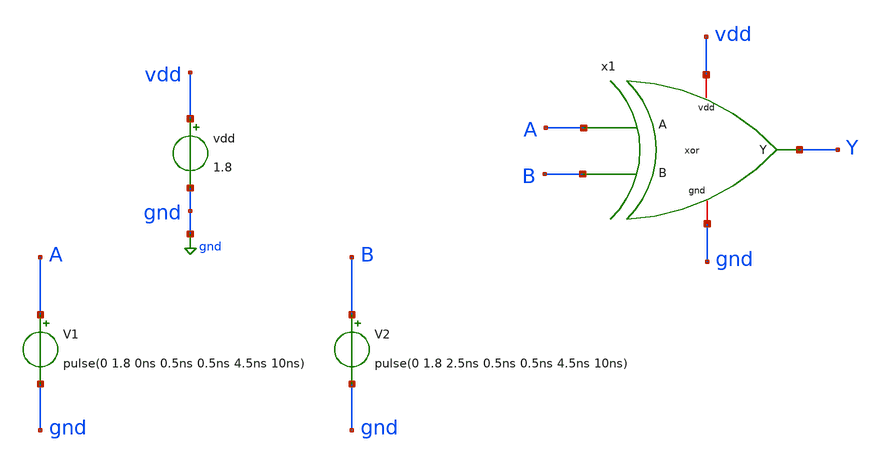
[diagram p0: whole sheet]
** sch_path: LogicGates/xor_tb.sch
**.subckt xor_tb
x1 vdd gnd A B Y xor
vdd vdd gnd 1.8
V1 A gnd pulse(0 1.8 0ns 0.5ns 0.5ns 4.5ns 10ns)
V2 B gnd pulse(0 1.8 2.5ns 0.5ns 0.5ns 4.5ns 10ns)
**** begin user architecture code


.lib /usr/local/share/pdk/sky130A/libs.tech/ngspice/sky130.lib.spice tt
.control
    tran 0.1n 100n
    plot A B
    plot Y
.endc

.save all

**** end user architecture code
**.ends

* expanding   symbol:  LogicGates/xor.sym # of pins=5
** sym_path: LogicGates/xor.sym
** sch_path: LogicGates/xor.sch
.subckt xor vdd gnd A B Y
*.ipin A
*.ipin B
*.iopin vdd
*.iopin gnd
*.opin Y
x1 vdd gnd A_c B net1 and
x2 vdd gnd A B_c net2 and
x3 vdd gnd net1 net2 Y or
x4 vdd gnd B B_c not
x5 vdd gnd A A_c not
.ends


* expanding   symbol:  LogicGates/and.sym # of pins=5
** sym_path: LogicGates/and.sym
** sch_path: LogicGates/and.sch
.subckt and vdd gnd A B Y
*.ipin A
*.ipin B
*.iopin vdd
*.iopin gnd
*.opin Y
XM1 net1 A net2 gnd sky130_fd_pr__nfet_01v8 L=0.15 W=1 nf=1 ad='int((nf+1)/2) * W/nf * 0.29' as='int((nf+2)/2) * W/nf * 0.29'
+ pd='2*int((nf+1)/2) * (W/nf + 0.29)' ps='2*int((nf+2)/2) * (W/nf + 0.29)' nrd='0.29 / W' nrs='0.29 / W'
+ sa=0 sb=0 sd=0 mult=1 m=1
XM2 net2 B gnd gnd sky130_fd_pr__nfet_01v8 L=0.15 W=1 nf=1 ad='int((nf+1)/2) * W/nf * 0.29' as='int((nf+2)/2) * W/nf * 0.29'
+ pd='2*int((nf+1)/2) * (W/nf + 0.29)' ps='2*int((nf+2)/2) * (W/nf + 0.29)' nrd='0.29 / W' nrs='0.29 / W'
+ sa=0 sb=0 sd=0 mult=1 m=1
XM3 net1 A vdd vdd sky130_fd_pr__pfet_01v8 L=0.15 W=2 nf=1 ad='int((nf+1)/2) * W/nf * 0.29' as='int((nf+2)/2) * W/nf * 0.29'
+ pd='2*int((nf+1)/2) * (W/nf + 0.29)' ps='2*int((nf+2)/2) * (W/nf + 0.29)' nrd='0.29 / W' nrs='0.29 / W'
+ sa=0 sb=0 sd=0 mult=1 m=1
XM4 net1 B vdd vdd sky130_fd_pr__pfet_01v8 L=0.15 W=2 nf=1 ad='int((nf+1)/2) * W/nf * 0.29' as='int((nf+2)/2) * W/nf * 0.29'
+ pd='2*int((nf+1)/2) * (W/nf + 0.29)' ps='2*int((nf+2)/2) * (W/nf + 0.29)' nrd='0.29 / W' nrs='0.29 / W'
+ sa=0 sb=0 sd=0 mult=1 m=1
x1 vdd gnd net1 Y not
.ends


* expanding   symbol:  LogicGates/or.sym # of pins=5
** sym_path: LogicGates/or.sym
** sch_path: LogicGates/or.sch
.subckt or vdd gnd A B Y
*.ipin A
*.ipin B
*.iopin vdd
*.iopin gnd
*.opin Y
XM1 net1 A gnd gnd sky130_fd_pr__nfet_01v8 L=0.15 W=1 nf=1 ad='int((nf+1)/2) * W/nf * 0.29' as='int((nf+2)/2) * W/nf * 0.29'
+ pd='2*int((nf+1)/2) * (W/nf + 0.29)' ps='2*int((nf+2)/2) * (W/nf + 0.29)' nrd='0.29 / W' nrs='0.29 / W'
+ sa=0 sb=0 sd=0 mult=1 m=1
XM2 net1 B gnd gnd sky130_fd_pr__nfet_01v8 L=0.15 W=1 nf=1 ad='int((nf+1)/2) * W/nf * 0.29' as='int((nf+2)/2) * W/nf * 0.29'
+ pd='2*int((nf+1)/2) * (W/nf + 0.29)' ps='2*int((nf+2)/2) * (W/nf + 0.29)' nrd='0.29 / W' nrs='0.29 / W'
+ sa=0 sb=0 sd=0 mult=1 m=1
XM3 net2 A vdd vdd sky130_fd_pr__pfet_01v8 L=0.15 W=2 nf=1 ad='int((nf+1)/2) * W/nf * 0.29' as='int((nf+2)/2) * W/nf * 0.29'
+ pd='2*int((nf+1)/2) * (W/nf + 0.29)' ps='2*int((nf+2)/2) * (W/nf + 0.29)' nrd='0.29 / W' nrs='0.29 / W'
+ sa=0 sb=0 sd=0 mult=1 m=1
XM4 net1 B net2 vdd sky130_fd_pr__pfet_01v8 L=0.15 W=2 nf=1 ad='int((nf+1)/2) * W/nf * 0.29' as='int((nf+2)/2) * W/nf * 0.29'
+ pd='2*int((nf+1)/2) * (W/nf + 0.29)' ps='2*int((nf+2)/2) * (W/nf + 0.29)' nrd='0.29 / W' nrs='0.29 / W'
+ sa=0 sb=0 sd=0 mult=1 m=1
x1 vdd gnd net1 Y not
.ends


* expanding   symbol:  LogicGates/not.sym # of pins=4
** sym_path: LogicGates/not.sym
** sch_path: LogicGates/not.sch
.subckt not vdd gnd vin vout
*.ipin vin
*.iopin vdd
*.iopin gnd
*.opin vout
XM2 vout vin vdd vdd sky130_fd_pr__pfet_01v8 L=0.15 W=2 nf=1 ad='int((nf+1)/2) * W/nf * 0.29' as='int((nf+2)/2) * W/nf * 0.29'
+ pd='2*int((nf+1)/2) * (W/nf + 0.29)' ps='2*int((nf+2)/2) * (W/nf + 0.29)' nrd='0.29 / W' nrs='0.29 / W'
+ sa=0 sb=0 sd=0 mult=1 m=1
XM1 vout vin gnd gnd sky130_fd_pr__nfet_01v8 L=0.15 W=1 nf=1 ad='int((nf+1)/2) * W/nf * 0.29' as='int((nf+2)/2) * W/nf * 0.29'
+ pd='2*int((nf+1)/2) * (W/nf + 0.29)' ps='2*int((nf+2)/2) * (W/nf + 0.29)' nrd='0.29 / W' nrs='0.29 / W'
+ sa=0 sb=0 sd=0 mult=1 m=1
.ends

.GLOBAL gnd
.end
